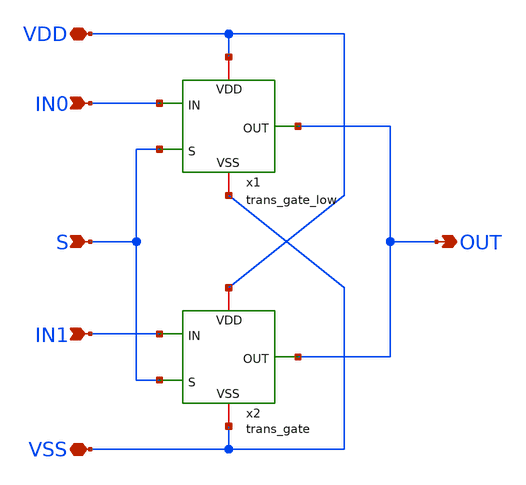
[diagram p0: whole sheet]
** sch_path: SSDOR_1V_v1/components/mux2/mux2.sch
**.subckt mux2 IN0 S IN1 VDD VSS OUT
*.ipin IN0
*.ipin S
*.ipin IN1
*.iopin VDD
*.iopin VSS
*.opin OUT
x1 OUT IN0 VDD S VSS trans_gate_low
x2 OUT IN1 VDD S VSS trans_gate
**.ends
.end
